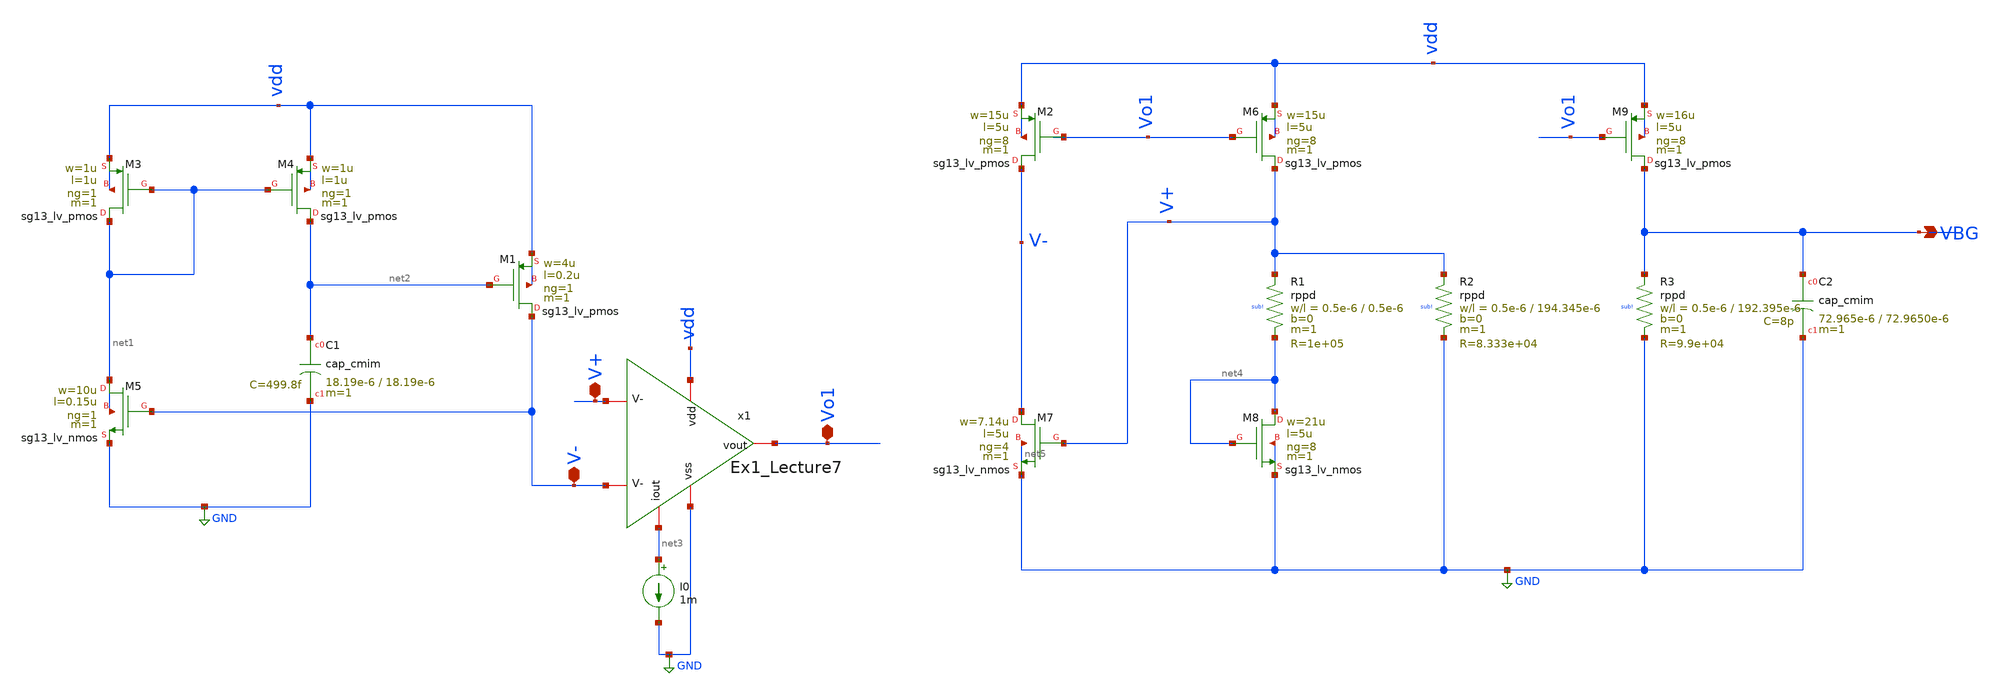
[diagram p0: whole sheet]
** sch_path: BTDay7-Ex/Ex2_Lecture7.sch
**.subckt Ex2_Lecture7 VBG Vo1 V+ V-
*.opin VBG
*.iopin Vo1
*.iopin V+
*.iopin V-
XM3 net1 net1 vdd vdd sg13_lv_pmos w=1u l=1u ng=1 m=1 mm_ok=1
XM4 net2 net1 vdd vdd sg13_lv_pmos w=1u l=1u ng=1 m=1 mm_ok=1
XM5 net1 V+ GND net1 sg13_lv_nmos w=10u l=0.15u ng=1 m=1 mm_ok=1
XM1 V+ net2 vdd vdd sg13_lv_pmos w=4u l=0.2u ng=1 m=1 mm_ok=1
XC1 net2 GND cap_cmim w=18.19e-6 l=18.19e-6 m=1 mm_ok=1
x1 vdd net3 V+ Vo1 GND Ex1_Lecture7
I0 net3 GND 1m
XM2 V- Vo1 vdd vdd sg13_lv_pmos w=15u l=5u ng=8 m=1 mm_ok=1
XM6 V+ Vo1 vdd vdd sg13_lv_pmos w=15u l=5u ng=8 m=1 mm_ok=1
XM7 V- V+ GND net5 sg13_lv_nmos w=7.14u l=5u ng=4 m=1 mm_ok=1
XM8 net4 net4 GND GND sg13_lv_nmos w=21u l=5u ng=8 m=1 mm_ok=1
XR1 V+ net4 sub! rppd w=0.5e-6 l=0.5e-6 m=1 b=0 mm_ok=1
XR2 V+ GND sub! rppd w=0.5e-6 l=194.345e-6 m=1 b=0 mm_ok=1
XM9 VBG Vo1 vdd vdd sg13_lv_pmos w=16u l=5u ng=8 m=1 mm_ok=1
XR3 VBG GND sub! rppd w=0.5e-6 l=192.395e-6 m=1 b=0 mm_ok=1
XC2 VBG GND cap_cmim w=72.965e-6 l=72.9650e-6 m=1 mm_ok=1
**.ends

* expanding   symbol:  /home/vietha/pdk/IHP-Open-PDK/ihp-sg13g2/libs.tech/Ex1_Lecture7.sym # of
*+ pins=6
** sym_path: BTDay7-Ex/Ex1_Lecture7.sym
** sch_path: BTDay7-Ex/Ex1_Lecture7.sch
.subckt Ex1_Lecture7 vdd iout V- vout vss
*.iopin vdd
*.iopin iout
*.iopin V-
*.iopin vss
*.iopin V-
*.iopin vout
XM6 iout iout vdd vdd sg13_lv_pmos w=75u l=2.08u ng=8 m=1 mm_ok=1
XM7 net1 iout vdd vdd sg13_lv_pmos w=5.3u l=1.95u ng=1 m=1 mm_ok=1
XM8 net3 V- net1 vdd sg13_lv_pmos w=7.41u l=3.64u ng=1 m=1 mm_ok=1
XM9 net2 V- net1 vdd sg13_lv_pmos w=7.41u l=3.64u ng=1 m=1 mm_ok=1
XM10 net3 net3 vss vss sg13_lv_nmos w=9.75u l=0.72u ng=1 m=1 mm_ok=1
XM11 net2 net3 vss vss sg13_lv_nmos w=9.75u l=0.72u ng=1 m=1 mm_ok=1
XM1 vout net2 vss vss sg13_lv_nmos w=9.75u l=28.8u ng=4 m=1 mm_ok=1
XM2 vout iout vdd vdd sg13_lv_pmos w=75u l=2.08u ng=8 m=1 mm_ok=1
XC1 net2 vout cap_cmim w=22.295e-6 l=22.295e-6 m=1 mm_ok=1
.ends

.GLOBAL GND
.end
